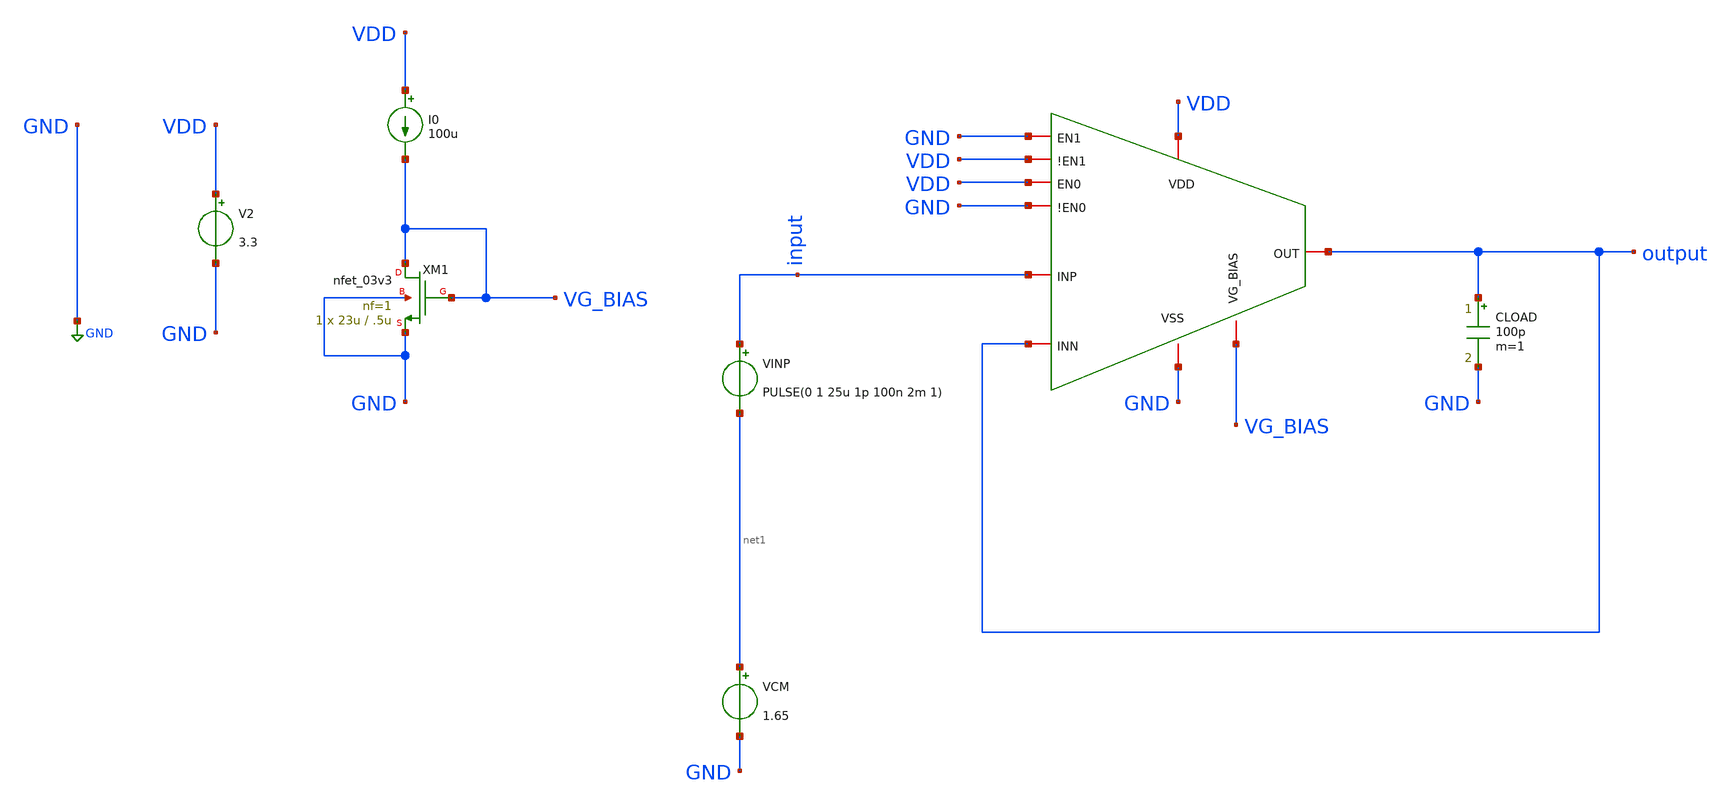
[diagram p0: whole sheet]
** sch_path: designs/libs/old_files/old_amps/ota_folded_cascode/programmable_tran_SR_tb.sch
**.subckt programmable_tran_SR_tb
x1 VDD VDD GND GND GND VDD output input output VG_BIAS programmable_folded
XM1 VG_BIAS VG_BIAS GND GND nfet_03v3 L=.5u W=23u nf=1 ad='int((nf+1)/2) * W/nf * 0.18u' as='int((nf+2)/2) * W/nf * 0.18u'
+ pd='2*int((nf+1)/2) * (W/nf + 0.18u)' ps='2*int((nf+2)/2) * (W/nf + 0.18u)' nrd='0.18u / W' nrs='0.18u / W'
+ sa=0 sb=0 sd=0 m=1
I0 VDD VG_BIAS 100u
V2 VDD GND 3.3
CLOAD output GND 100p m=1
VINP input net1 PULSE(0 1 25u 1p 100n 2m 1)
VCM net1 GND 1.65
**** begin user architecture code

.include $::180MCU_MODELS/design.ngspice
.lib $::180MCU_MODELS/sm141064.ngspice typical



.control
tran 1n 100u
meas tran v_before find v(output) at=24u
meas tran v_after find v(output) at=90u
let v_20 = v_before + 0.2 * (v_after - v_before)
let v_80 = v_before + 0.8 * (v_after - v_before)
meas tran t_20 when v(output) = v_20 rise = 1 from = 25u
meas tran t_80 when v(output) = v_80 rise = 1 from = 25u
let slew_rate = (v_80 - v_20) / (t_80 - t_20)
print v_before v_after
print slew_rate

plot v(input) v(output)
.endc



**** end user architecture code
**.ends
.GLOBAL GND
.end
